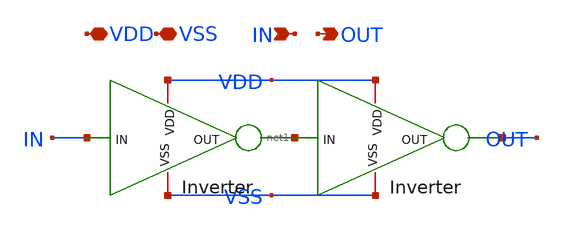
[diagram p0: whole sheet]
** sch_path: DAC_PAKISTAN_01/Pakistan1_Xschem/INV_BUFF.sch
**.subckt INV_BUFF OUT VDD VSS IN
*.opin OUT
*.iopin VDD
*.iopin VSS
*.ipin IN
x1 VSS VDD net1 IN Inverter
x2 VSS VDD OUT net1 Inverter
**.ends

* expanding   symbol:  Inverter.sym # of pins=4
** sym_path: DAC_PAKISTAN_01/Pakistan1_Xschem/Inverter.sym
** sch_path: DAC_PAKISTAN_01/Pakistan1_Xschem/Inverter.sch
.subckt Inverter VSS VDD OUT IN
*.iopin VDD
*.iopin VSS
*.ipin IN
*.opin OUT
XM1 OUT IN VSS VSS nfet_03v3 L=0.28u W=0.25u nf=1 ad='int((nf+1)/2) * W/nf * 0.18u' as='int((nf+2)/2) * W/nf * 0.18u'
+ pd='2*int((nf+1)/2) * (W/nf + 0.18u)' ps='2*int((nf+2)/2) * (W/nf + 0.18u)' nrd='0.18u / W' nrs='0.18u / W'
+ sa=0 sb=0 sd=0 m=1
XM2 OUT IN VDD VDD pfet_03v3 L=0.28u W=0.5u nf=1 ad='int((nf+1)/2) * W/nf * 0.18u' as='int((nf+2)/2) * W/nf * 0.18u'
+ pd='2*int((nf+1)/2) * (W/nf + 0.18u)' ps='2*int((nf+2)/2) * (W/nf + 0.18u)' nrd='0.18u / W' nrs='0.18u / W'
+ sa=0 sb=0 sd=0 m=1
.ends

.end
